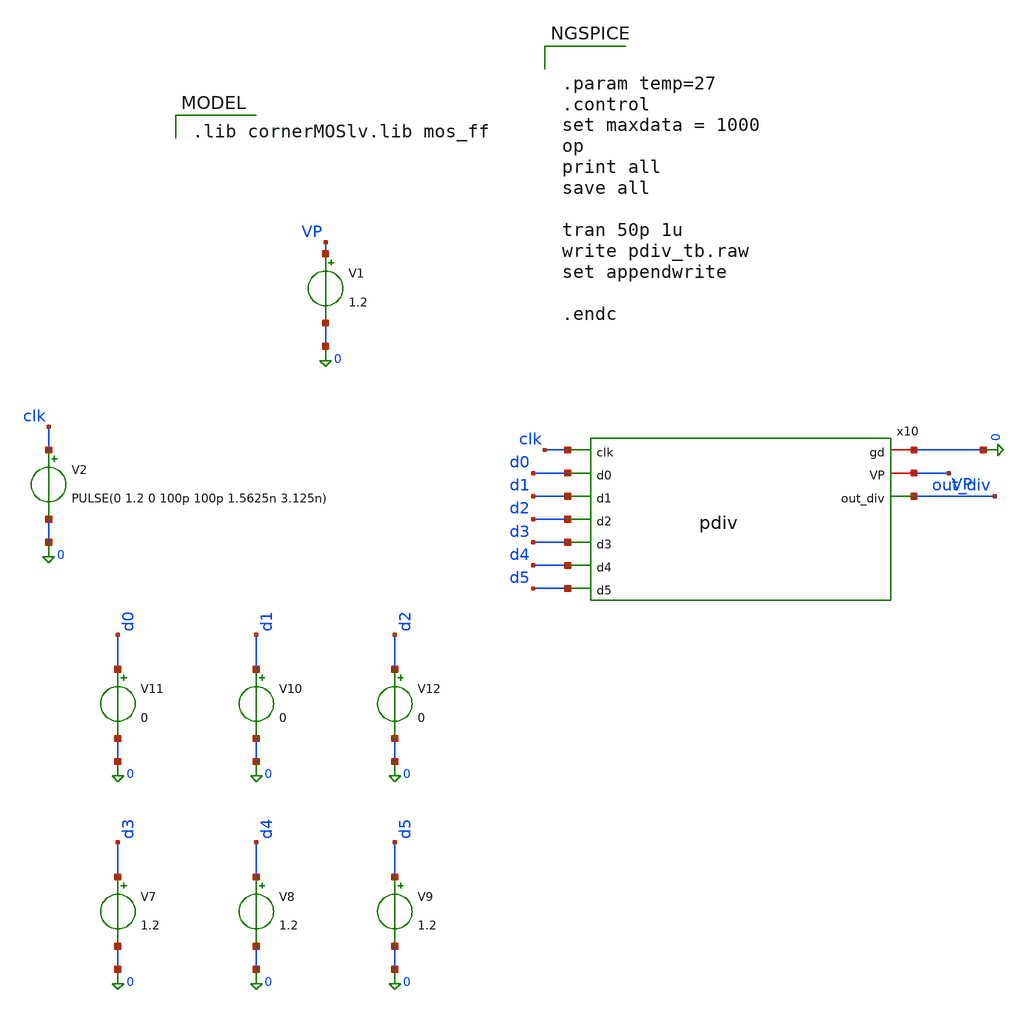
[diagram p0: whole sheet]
** sch_path: schematics/divider/tb/pdiv_tb.sch
**.subckt pdiv_tb
V1 VP 0 1.2
V2 clk 0 PULSE(0 1.2 0 100p 100p 1.5625n 3.125n)
V8 d4 0 1.2
V9 d5 0 1.2
V11 d0 0 0
V10 d1 0 0
V12 d2 0 0
V7 d3 0 1.2
x10 0 VP clk d0 d1 d2 d3 d4 d5 out_div pdiv
**** begin user architecture code
 .lib cornerMOSlv.lib mos_ff



.param temp=27
.control
set maxdata = 1000
op
print all
save all

tran 50p 1u
write pdiv_tb.raw
set appendwrite

.endc


**** end user architecture code
**.ends
.end
